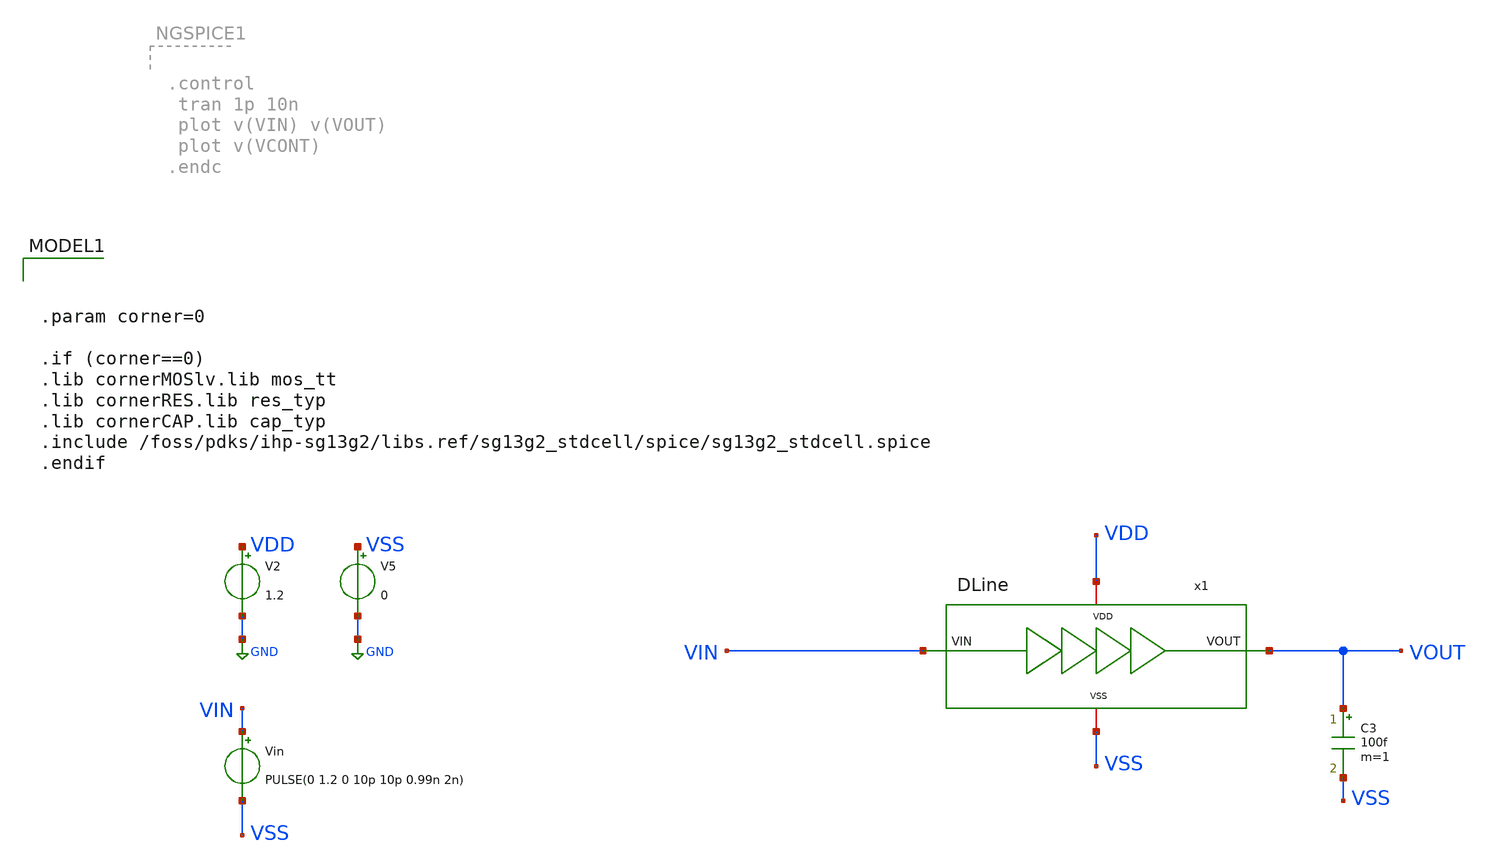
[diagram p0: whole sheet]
** sch_path: xschem/testbenchs/tb_large_delay.sch
* IHP-GmbH/IHP-Open-PDK/ihp-sg13g2/libs.tech/xschem/sg13g2_stdcells/sg13g2_inv_16.sch:
* Copyright 2023 IHP PDK Authors
* Licensed under the Apache License, Version 2.0 (the "License");
**.subckt tb_large_delay
Vin VIN VSS PULSE(0 1.2 0 10p 10p 0.99n 2n)
C3 VOUT VSS 100f m=1
V2 VDD GND 1.2
V5 VSS GND 0
x1 VSS VDD VIN VOUT DLine
**** begin user architecture code


.param corner=0

.if (corner==0)
.lib cornerMOSlv.lib mos_tt
.lib cornerRES.lib res_typ
.lib cornerCAP.lib cap_typ
.include /foss/pdks/ihp-sg13g2/libs.ref/sg13g2_stdcell/spice/sg13g2_stdcell.spice
.endif



.control
* ---- settings you tweak ----


   * ---- user settings ----
  let vlow  = 0
  let vhigh = 1.2
  let v50   = vlow + 0.5*(vhigh - vlow)

  let start_edge = 0     ; skip early edges (settling)
  let N = 200             ; number of phase samples



  tran 2p 200n

  * ---- allocate vectors ----
  let tvec   = vector(N)
  let phivec = vector(N)

  let k = 0
  let i = start_edge

  while k < N
    * crossing times
    meas tran tin      WHEN v(VIN)=v50  RISE=i
    meas tran tout     WHEN v(VOUT)=v50 RISE=i
    meas tran tin_next WHEN v(VIN)=v50  RISE=(i+1)

    * delay + period
    let dt = tout - tin
    let T  = tin_next - tin

    * phase in degrees (per-cycle)
    let phi = 360*dt/T
    let phi = phi - 360*floor(phi/360)

    * store sample at time = tin
    let tvec[k]   = tin
    let phivec[k] = phi

    let k = k + 1
    let i = i + 1
  end

  * plot phase vs time (one point per cycle)
  plot phivec vs tvec
  *plot v(VCONT)
  plot v(VIN) v(VOUT)
.endc


**** end user architecture code
**.ends

* expanding   symbol:  /foss/designs/DLL/2026/Cells/DLine.sym # of pins=4
** sym_path: /foss/designs/DLL/2026/Cells/DLine.sym
** sch_path: /foss/designs/DLL/2026/Cells/DLine.sch
.subckt DLine VSS VDD VIN VOUT
*.opin VOUT
*.ipin VIN
*.iopin VDD
*.iopin VSS
x7 net2 net1 VDD VSS sg13g2_dlygate4sd1_1
x1 net2 net1 VDD VSS sg13g2_dlygate4sd1_1
x2 net3 net2 VDD VSS sg13g2_inv_4
x3 net4 net3 VDD VSS sg13g2_inv_8
x4 VOUT net4 VDD VSS sg13g2_inv_16
x5 net1 net7 VDD VSS sg13g2_dlygate4sd1_1
x6 net7 net6 VDD VSS sg13g2_dlygate4sd1_1
x8 net6 net5 VDD VSS sg13g2_dlygate4sd1_1
x9 net5 VIN VDD VSS sg13g2_dlygate4sd1_1
.ends


* expanding   symbol:  sg13g2_stdcells/sg13g2_dlygate4sd1_1.sym # of pins=2
** sym_path: sg13g2_stdcells/sg13g2_dlygate4sd1_1.sym
** sch_path: sg13g2_stdcells/sg13g2_dlygate4sd1_1.sch
.subckt sg13g2_dlygate4sd1_1 X A VDD VSS
*.ipin A
*.opin X
*.iopin VDD
*.iopin VSS
XM1 net2 A VSS VSS sg13_lv_nmos w=420.00n l=130.00n ng=1 m=1 mm_ok=1
XM2 net1 net2 VSS VSS sg13_lv_nmos w=420.00n l=130.00n ng=1 m=1 mm_ok=1
XM3 net3 net1 VSS VSS sg13_lv_nmos w=420.00n l=130.00n ng=1 m=1 mm_ok=1
XM4 X net3 VSS VSS sg13_lv_nmos w=740.00n l=130.00n ng=1 m=1 mm_ok=1
XM5 net2 A VDD VDD sg13_lv_pmos w=420.00n l=130.00n ng=1 m=1 mm_ok=1
XM6 net1 net2 VDD VDD sg13_lv_pmos w=1.000u l=130.00n ng=1 m=1 mm_ok=1
XM7 net3 net1 VDD VDD sg13_lv_pmos w=1.000u l=130.00n ng=1 m=1 mm_ok=1
XM8 X net3 VDD VDD sg13_lv_pmos w=1.12u l=130.00n ng=1 m=1 mm_ok=1
.ends


* expanding   symbol:  sg13g2_stdcells/sg13g2_inv_2.sym # of pins=2
** sym_path: sg13g2_stdcells/sg13g2_inv_2.sym
** sch_path: sg13g2_stdcells/sg13g2_inv_2.sch
.subckt sg13g2_inv_2 Y A VDD VSS
*.opin Y
*.ipin A
*.iopin VDD
*.iopin VSS
XM1 Y A VSS VSS sg13_lv_nmos w=1.48u l=130.00n ng=2 m=1 mm_ok=1
XM2 Y A VDD VDD sg13_lv_pmos w=2.24u l=130.00n ng=2 m=1 mm_ok=1
.ends


* expanding   symbol:  sg13g2_stdcells/sg13g2_inv_4.sym # of pins=2
** sym_path: sg13g2_stdcells/sg13g2_inv_4.sym
** sch_path: sg13g2_stdcells/sg13g2_inv_4.sch
.subckt sg13g2_inv_4 Y A VDD VSS
*.ipin A
*.opin Y
*.iopin VDD
*.iopin VSS
XM1 Y A VSS VSS sg13_lv_nmos w=2.96u l=130.00n ng=4 m=1 mm_ok=1
XM2 Y A VDD VDD sg13_lv_pmos w=4.48u l=130.00n ng=4 m=1 mm_ok=1
.ends


* expanding   symbol:  sg13g2_stdcells/sg13g2_inv_8.sym # of pins=2
** sym_path: sg13g2_stdcells/sg13g2_inv_8.sym
** sch_path: sg13g2_stdcells/sg13g2_inv_8.sch
.subckt sg13g2_inv_8 Y A VDD VSS
*.opin Y
*.ipin A
*.iopin VDD
*.iopin VSS
XM1 Y A VSS VSS sg13_lv_nmos w=5.92u l=130.00n ng=8 m=1 mm_ok=1
XM2 Y A VDD VDD sg13_lv_pmos w=8.96u l=130.00n ng=8 m=1 mm_ok=1
.ends


* expanding   symbol:  sg13g2_stdcells/sg13g2_inv_16.sym # of pins=2
** sym_path: sg13g2_stdcells/sg13g2_inv_16.sym
** sch_path: sg13g2_stdcells/sg13g2_inv_16.sch
.subckt sg13g2_inv_16 Y A VDD VSS
*.opin Y
*.iopin VSS
*.ipin A
*.iopin VDD
XM1 Y A VSS VSS sg13_lv_nmos w=11.84u l=130.00n ng=16 m=1 mm_ok=1
XM2 Y A VDD VDD sg13_lv_pmos w=17.92u l=130.00n ng=16 m=1 mm_ok=1
.ends

.GLOBAL GND
.end
